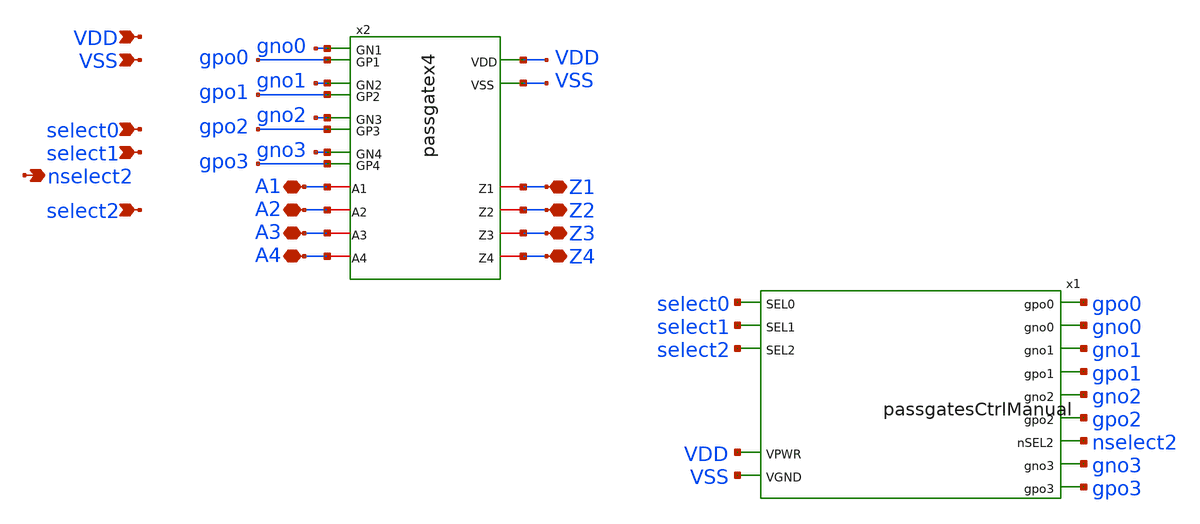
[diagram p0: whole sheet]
** sch_path: xschem/mux4onehot_b.sch
**.subckt mux4onehot_b select0 select1 select2 A1 A2 A3 A4 Z1 Z2 Z3 Z4 nselect2 VDD VSS
*.ipin select0
*.ipin select1
*.ipin select2
*.iopin A1
*.iopin A2
*.iopin A3
*.iopin A4
*.iopin Z1
*.iopin Z2
*.iopin Z3
*.iopin Z4
*.opin nselect2
*.ipin VDD
*.ipin VSS
x2 gpo2 gpo1 gpo0 VDD gpo3 VSS A3 A2 A1 Z3 Z1 Z2 A4 Z4 gno2 gno1 gno0 gno3 passgatex4
x1 gpo0 gno0 gno1 gpo1 select0 select1 gno2 gpo2 nselect2 select2 gno3 gpo3 VDD VSS
+ passgatesCtrlManual
**.ends
.end
